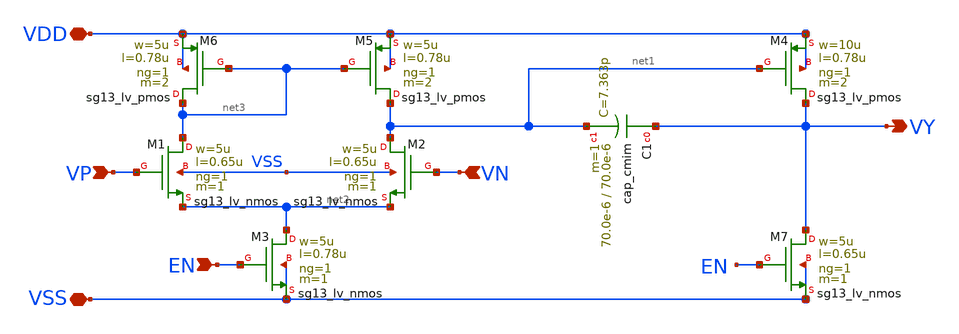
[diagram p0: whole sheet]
** sch_path: libs/core_analog/core_ota/schematics/2-stage-miller.sch
**.subckt 2-stage-miller VP VN VY VSS VDD EN
*.ipin VP
*.ipin VN
*.opin VY
*.iopin VSS
*.iopin VDD
*.ipin EN
XM1 net3 VP net2 VSS sg13_lv_nmos w=5u l=0.65u ng=1 m=1 mm_ok=1
XM2 net1 VN net2 VSS sg13_lv_nmos w=5u l=0.65u ng=1 m=1 mm_ok=1
XM5 net1 net3 VDD VDD sg13_lv_pmos w=5u l=0.78u ng=1 m=2 mm_ok=1
XM6 net3 net3 VDD VDD sg13_lv_pmos w=5u l=0.78u ng=1 m=2 mm_ok=1
XM3 net2 EN VSS VSS sg13_lv_nmos w=5u l=0.78u ng=1 m=1 mm_ok=1
XC1 VY net1 cap_cmim w=70.0e-6 l=70.0e-6 m=1 mm_ok=1
XM4 VY net1 VDD VDD sg13_lv_pmos w=10u l=0.78u ng=1 m=2 mm_ok=1
XM7 VY EN VSS VSS sg13_lv_nmos w=5u l=0.65u ng=1 m=1 mm_ok=1
**.ends
.end
